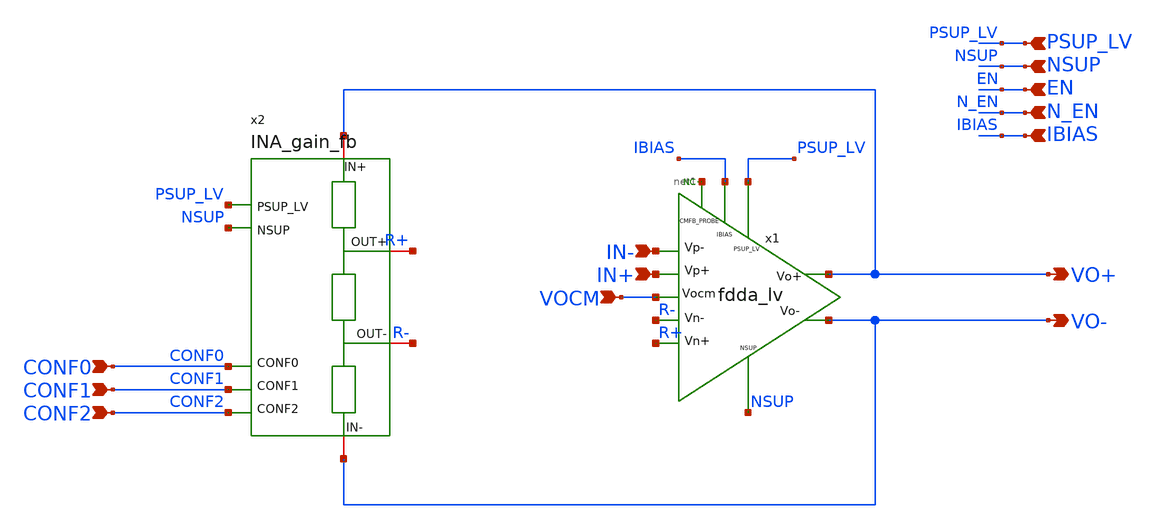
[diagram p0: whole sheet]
** sch_path: xschem/blocks/INA/INA.sch
**.subckt INA VO+ VO- NSUP EN N_EN IBIAS PSUP_LV CONF0 CONF1 VOCM IN- IN+ CONF2
*.opin VO+
*.opin VO-
*.ipin NSUP
*.ipin EN
*.ipin N_EN
*.ipin IBIAS
*.ipin PSUP_LV
*.ipin CONF0
*.ipin CONF1
*.ipin VOCM
*.ipin IN-
*.ipin IN+
*.ipin CONF2
* noconn #net1
x1 PSUP_LV IN- R- R+ IN+ VO+ VO- IBIAS NSUP net1 VOCM fdda_lv
x2 VO+ R+ PSUP_LV NSUP CONF1 CONF0 R- VO- CONF2 INA_gain_fb
**.ends
.end
